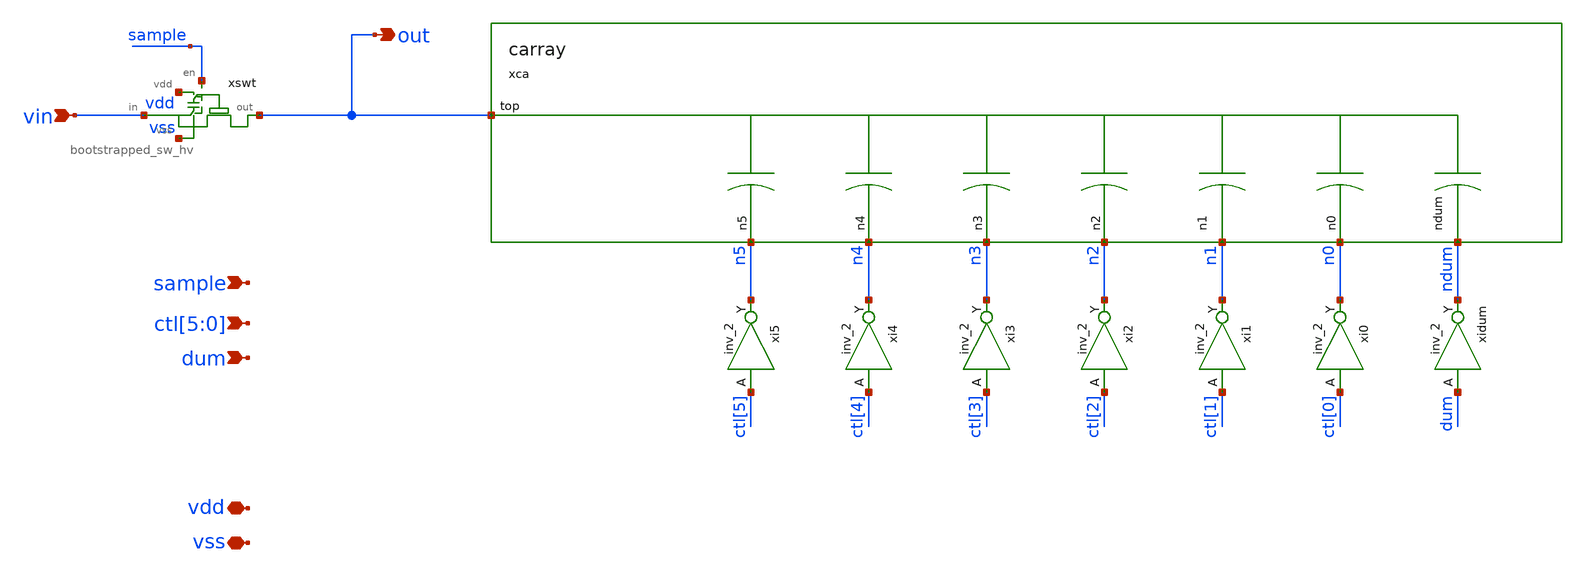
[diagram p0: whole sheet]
** sch_path: xschem/sar_10b/dac/dac.sch
**.subckt dac vin sample out ctl[5],ctl[4],ctl[3],ctl[2],ctl[1],ctl[0] dum vdd vss
*.ipin vin
*.ipin sample
*.opin out
*.ipin ctl[5],ctl[4],ctl[3],ctl[2],ctl[1],ctl[0]
*.ipin dum
*.iopin vdd
*.iopin vss
xca out n0 n5 n4 n2 ndum n3 n1 carray
xswt out sample vdd vin vss bootstrapped_sw_hv
xidum dum vss vss vdd vdd ndum sky130_fd_sc_hd__inv_2
xi0 ctl[0] vss vss vdd vdd n0 sky130_fd_sc_hd__inv_2
xi1 ctl[1] vss vss vdd vdd n1 sky130_fd_sc_hd__inv_2
xi2 ctl[2] vss vss vdd vdd n2 sky130_fd_sc_hd__inv_2
xi3 ctl[3] vss vss vdd vdd n3 sky130_fd_sc_hd__inv_2
xi4 ctl[4] vss vss vdd vdd n4 sky130_fd_sc_hd__inv_2
xi5 ctl[5] vss vss vdd vdd n5 sky130_fd_sc_hd__inv_2
**.ends
.end
